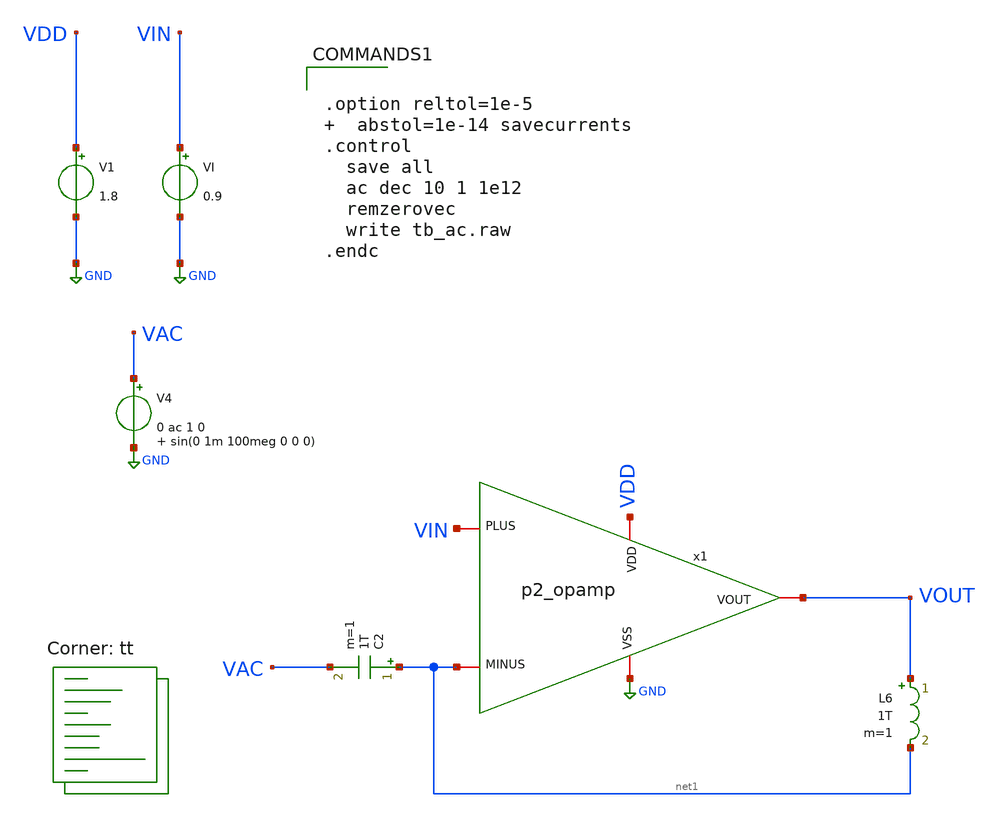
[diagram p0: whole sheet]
** sch_path: xschem/tb_ac.sch
**.subckt tb_ac
x1 VDD net1 VIN VOUT GND p2_opamp
V1 VDD GND 1.8
VI VIN GND 0.9
C2 net1 VAC 1T m=1
L6 VOUT net1 1T m=1
V4 VAC GND 0 ac 1 0 sin(0 1m 100meg 0 0 0)
**** begin user architecture code
.lib $::SKYWATER_MODELS/sky130.lib.spice tt


.option reltol=1e-5   abstol=1e-14 savecurrents
.control
  save all
  ac dec 10 1 1e12
  remzerovec
  write tb_ac.raw
.endc


**** end user architecture code
**.ends

* expanding   symbol:  p2_opamp.sym # of pins=5
** sym_path: xschem/p2_opamp.sym
** sch_path: xschem/p2_opamp.sch
.subckt p2_opamp VDD MINUS PLUS VOUT VSS
*.iopin VDD
*.iopin VSS
*.iopin PLUS
*.iopin MINUS
*.iopin VOUT
XM2 net2 MINUS net1 VSS sky130_fd_pr__nfet_01v8 L=0.15 W=16 nf=1 ad='int((nf+1)/2) * W/nf * 0.29' as='int((nf+2)/2) * W/nf * 0.29'
+ pd='2*int((nf+1)/2) * (W/nf + 0.29)' ps='2*int((nf+2)/2) * (W/nf + 0.29)' nrd='0.29 / W' nrs='0.29 / W'
+ sa=0 sb=0 sd=0 mult=1 m=1
XM1 net4 PLUS net1 VSS sky130_fd_pr__nfet_01v8 L=0.15 W=16 nf=1 ad='int((nf+1)/2) * W/nf * 0.29' as='int((nf+2)/2) * W/nf * 0.29'
+ pd='2*int((nf+1)/2) * (W/nf + 0.29)' ps='2*int((nf+2)/2) * (W/nf + 0.29)' nrd='0.29 / W' nrs='0.29 / W'
+ sa=0 sb=0 sd=0 mult=1 m=1
XM3 net1 net3 VSS VSS sky130_fd_pr__nfet_01v8 L=0.15 W=4 nf=1 ad='int((nf+1)/2) * W/nf * 0.29' as='int((nf+2)/2) * W/nf * 0.29'
+ pd='2*int((nf+1)/2) * (W/nf + 0.29)' ps='2*int((nf+2)/2) * (W/nf + 0.29)' nrd='0.29 / W' nrs='0.29 / W'
+ sa=0 sb=0 sd=0 mult=1 m=1
XM4 net2 net2 VDD VDD sky130_fd_pr__pfet_01v8 L=0.15 W=32 nf=1 ad='int((nf+1)/2) * W/nf * 0.29' as='int((nf+2)/2) * W/nf * 0.29'
+ pd='2*int((nf+1)/2) * (W/nf + 0.29)' ps='2*int((nf+2)/2) * (W/nf + 0.29)' nrd='0.29 / W' nrs='0.29 / W'
+ sa=0 sb=0 sd=0 mult=1 m=1
XM5 net4 net2 VDD VDD sky130_fd_pr__pfet_01v8 L=0.15 W=32 nf=1 ad='int((nf+1)/2) * W/nf * 0.29' as='int((nf+2)/2) * W/nf * 0.29'
+ pd='2*int((nf+1)/2) * (W/nf + 0.29)' ps='2*int((nf+2)/2) * (W/nf + 0.29)' nrd='0.29 / W' nrs='0.29 / W'
+ sa=0 sb=0 sd=0 mult=1 m=1
XM6 net3 net3 VSS VSS sky130_fd_pr__nfet_01v8 L=0.15 W=1 nf=1 ad='int((nf+1)/2) * W/nf * 0.29' as='int((nf+2)/2) * W/nf * 0.29'
+ pd='2*int((nf+1)/2) * (W/nf + 0.29)' ps='2*int((nf+2)/2) * (W/nf + 0.29)' nrd='0.29 / W' nrs='0.29 / W'
+ sa=0 sb=0 sd=0 mult=1 m=1
XM7 VOUT net3 VSS VSS sky130_fd_pr__nfet_01v8 L=0.15 W=8 nf=1 ad='int((nf+1)/2) * W/nf * 0.29' as='int((nf+2)/2) * W/nf * 0.29'
+ pd='2*int((nf+1)/2) * (W/nf + 0.29)' ps='2*int((nf+2)/2) * (W/nf + 0.29)' nrd='0.29 / W' nrs='0.29 / W'
+ sa=0 sb=0 sd=0 mult=1 m=1
XM8 VOUT net4 VDD VDD sky130_fd_pr__pfet_01v8 L=0.15 W=40 nf=1 ad='int((nf+1)/2) * W/nf * 0.29' as='int((nf+2)/2) * W/nf * 0.29'
+ pd='2*int((nf+1)/2) * (W/nf + 0.29)' ps='2*int((nf+2)/2) * (W/nf + 0.29)' nrd='0.29 / W' nrs='0.29 / W'
+ sa=0 sb=0 sd=0 mult=1 m=1
XC1 VOUT net4 sky130_fd_pr__cap_mim_m3_2 W=1 L=1 MF=1 m=1
XR1 net3 VDD VSS sky130_fd_pr__res_xhigh_po_5p73 L=150 mult=1 m=1
.ends

.GLOBAL GND
.end
